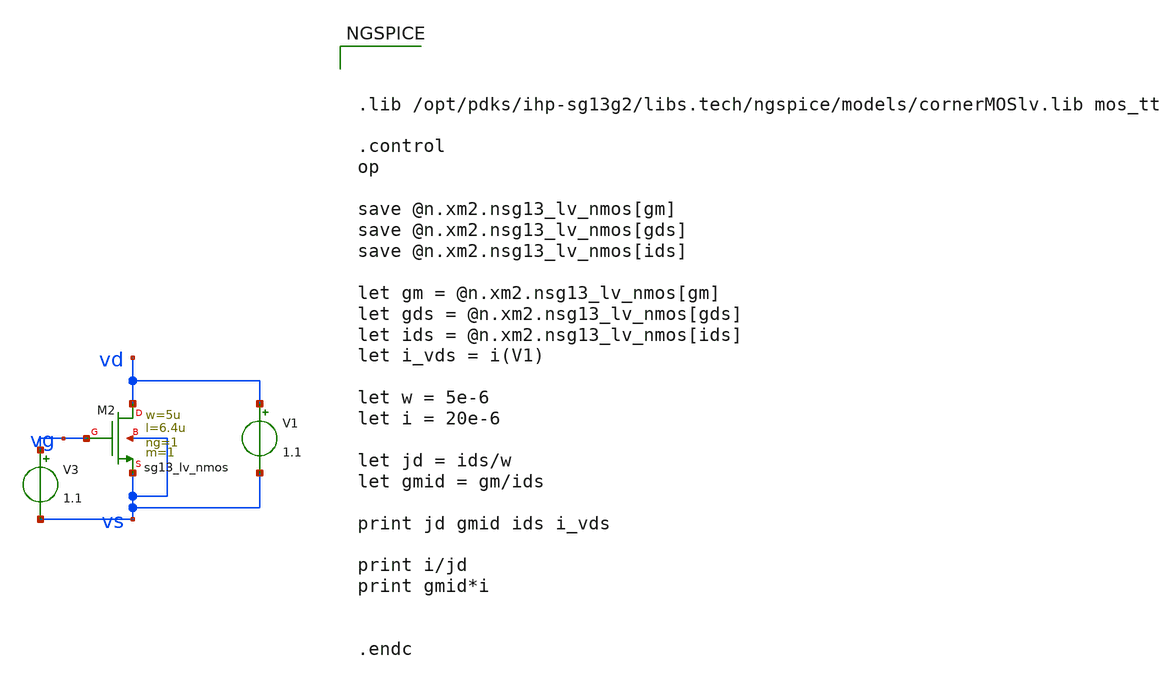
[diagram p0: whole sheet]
** sch_path: test/transitor/xschem/nmos_sweep.sch
**.subckt nmos_sweep
XM2 vd vg vs vs sg13_lv_nmos w=5u l=6.4u ng=1 m=1 mm_ok=1
V1 vd vs 1.1
V3 vg vs 1.1
**** begin user architecture code



.lib /opt/pdks/ihp-sg13g2/libs.tech/ngspice/models/cornerMOSlv.lib mos_tt

.control
op

save @n.xm2.nsg13_lv_nmos[gm]
save @n.xm2.nsg13_lv_nmos[gds]
save @n.xm2.nsg13_lv_nmos[ids]

let gm = @n.xm2.nsg13_lv_nmos[gm]
let gds = @n.xm2.nsg13_lv_nmos[gds]
let ids = @n.xm2.nsg13_lv_nmos[ids]
let i_vds = i(V1)

let w = 5e-6
let i = 20e-6

let jd = ids/w
let gmid = gm/ids

print jd gmid ids i_vds

print i/jd
print gmid*i


.endc



**** end user architecture code
**.ends
.end
